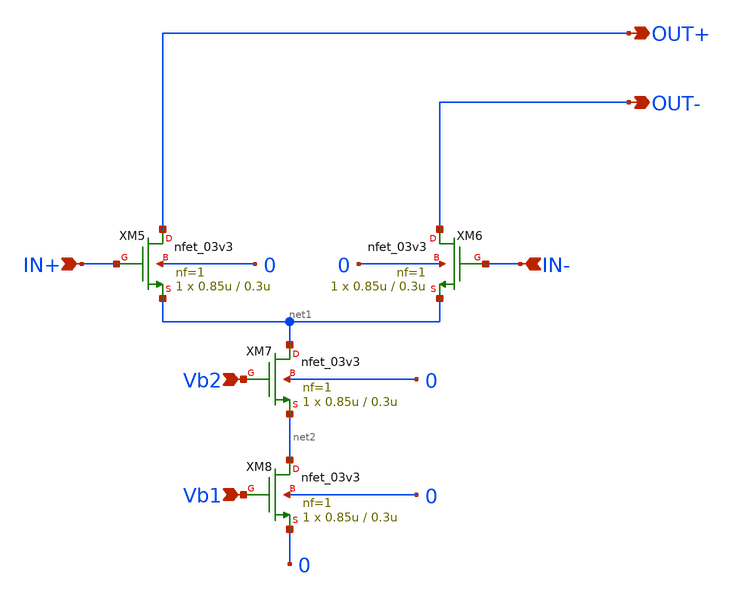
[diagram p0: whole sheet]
** sch_path: initial_notebooks_2023/accepted_notebooks/Current-Steering-DAC/DAC/current_unitx1.sch
**.subckt current_unitx1 IN+ IN- Vb2 Vb1 OUT+ OUT-
*.ipin IN+
*.ipin IN-
*.ipin Vb2
*.ipin Vb1
*.opin OUT+
*.opin OUT-
XM5 OUT+ IN+ net1 0 nfet_03v3 L=0.3u W=0.85u nf=1 ad='int((nf+1)/2) * W/nf * 0.18u' as='int((nf+2)/2) * W/nf * 0.18u'
+ pd='2*int((nf+1)/2) * (W/nf + 0.18u)' ps='2*int((nf+2)/2) * (W/nf + 0.18u)' nrd='0.18u / W' nrs='0.18u / W'
+ sa=0 sb=0 sd=0 m=1
XM6 OUT- IN- net1 0 nfet_03v3 L=0.3u W=0.85u nf=1 ad='int((nf+1)/2) * W/nf * 0.18u' as='int((nf+2)/2) * W/nf * 0.18u'
+ pd='2*int((nf+1)/2) * (W/nf + 0.18u)' ps='2*int((nf+2)/2) * (W/nf + 0.18u)' nrd='0.18u / W' nrs='0.18u / W'
+ sa=0 sb=0 sd=0 m=1
XM7 net1 Vb2 net2 0 nfet_03v3 L=0.3u W=0.85u nf=1 ad='int((nf+1)/2) * W/nf * 0.18u' as='int((nf+2)/2) * W/nf * 0.18u'
+ pd='2*int((nf+1)/2) * (W/nf + 0.18u)' ps='2*int((nf+2)/2) * (W/nf + 0.18u)' nrd='0.18u / W' nrs='0.18u / W'
+ sa=0 sb=0 sd=0 m=1
XM8 net2 Vb1 0 0 nfet_03v3 L=0.3u W=0.85u nf=1 ad='int((nf+1)/2) * W/nf * 0.18u' as='int((nf+2)/2) * W/nf * 0.18u'
+ pd='2*int((nf+1)/2) * (W/nf + 0.18u)' ps='2*int((nf+2)/2) * (W/nf + 0.18u)' nrd='0.18u / W' nrs='0.18u / W'
+ sa=0 sb=0 sd=0 m=1
**.ends
.end
